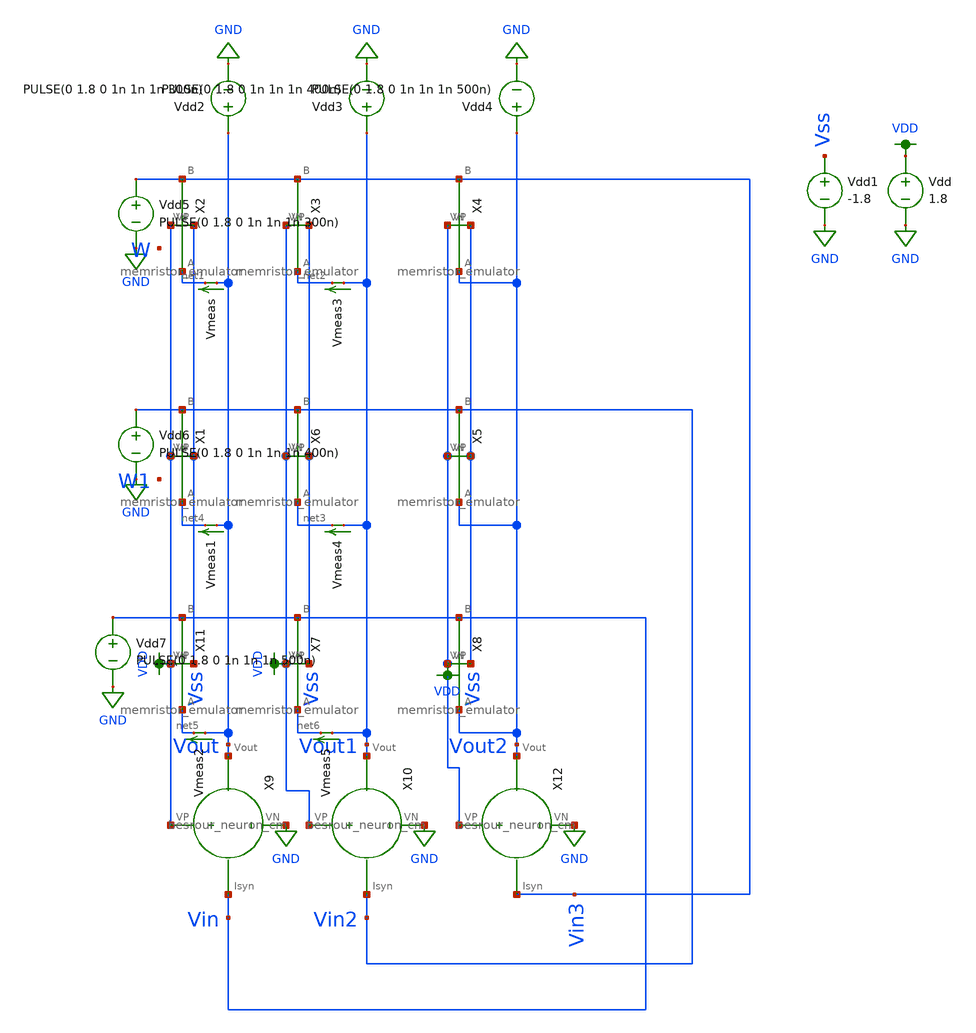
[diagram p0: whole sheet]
** sch_path: schematic/crossbar.sch
**.subckt crossbar
Vdd VDD GND 1.8
Vdd1 Vss GND -1.8
X11 VDD Vss Vin net5 memristor_emulator
X1 VDD Vss Vin2 net4 memristor_emulator
X2 VDD Vss Vin3 net1 memristor_emulator
X3 VDD Vss Vin3 net2 memristor_emulator
X4 VDD Vss Vin3 Vout2 memristor_emulator
X5 VDD Vss Vin2 Vout2 memristor_emulator
X6 VDD Vss Vin2 net3 memristor_emulator
X7 VDD Vss Vin net6 memristor_emulator
X8 VDD Vss Vin Vout2 memristor_emulator
X9 Vin Vout VDD GND besrour_neuron_cm
X10 Vin2 Vout1 VDD GND besrour_neuron_cm
X12 Vin3 Vout2 VDD GND besrour_neuron_cm
Vdd2 Vout GND PULSE(0 1.8 0 1n 1n 1n 300n)
Vdd3 Vout1 GND PULSE(0 1.8 0 1n 1n 1n 400n)
Vdd4 Vout2 GND PULSE(0 1.8 0 1n 1n 1n 500n)
Vdd5 Vin3 GND PULSE(0 1.8 0 1n 1n 1n 300n)
Vdd6 Vin2 GND PULSE(0 1.8 0 1n 1n 1n 400n)
Vdd7 Vin GND PULSE(0 1.8 0 1n 1n 1n 500n)
Vmeas Vout net1 0
.save i(vmeas)
Vmeas1 Vout net4 0
.save i(vmeas1)
Vmeas2 Vout net5 0
.save i(vmeas2)
Vmeas3 Vout1 net2 0
.save i(vmeas3)
Vmeas4 Vout1 net3 0
.save i(vmeas4)
Vmeas5 Vout1 net6 0
.save i(vmeas5)
**** begin user architecture code

.option wnflag=1
.param MC_SWITCH=0.0
.lib ~/skywater/skywater-pdk/libraries/sky130_fd_pr_ngspice/latest/models/sky130.lib.spice tt


.param W=12
.param L=0.5
.tran 1n 100u
.save all

**** end user architecture code
**.ends

* expanding   symbol:  /home/madvlsi/neuromorphic_computing_final/schematic/memristor_emulator.sym #
*+ of pins=4
** sym_path: schematic/memristor_emulator.sym
** sch_path: schematic/memristor_emulator.sch
.subckt memristor_emulator VP VN B A
*.ipin A
*.iopin VN
*.iopin VP
*.opin B
XM1 B in_cap A B sky130_fd_pr__pfet_01v8 L=0.3 W=12 nf=1 ad='int((nf+1)/2) * W/nf * 0.29' as='int((nf+2)/2) * W/nf * 0.29'
+ pd='2*int((nf+1)/2) * (W/nf + 0.29)' ps='2*int((nf+2)/2) * (W/nf + 0.29)' nrd='0.29 / W' nrs='0.29 / W'
+ sa=0 sb=0 sd=0 mult=1 m=1
XM2 VP A in_cap VP sky130_fd_pr__pfet_01v8 L=2 W=3 nf=1 ad='int((nf+1)/2) * W/nf * 0.29' as='int((nf+2)/2) * W/nf * 0.29'
+ pd='2*int((nf+1)/2) * (W/nf + 0.29)' ps='2*int((nf+2)/2) * (W/nf + 0.29)' nrd='0.29 / W' nrs='0.29 / W'
+ sa=0 sb=0 sd=0 mult=1 m=1
XM3 VN in_cap VN VN sky130_fd_pr__nfet_01v8 L=20 W=20 nf=1 ad='int((nf+1)/2) * W/nf * 0.29' as='int((nf+2)/2) * W/nf * 0.29'
+ pd='2*int((nf+1)/2) * (W/nf + 0.29)' ps='2*int((nf+2)/2) * (W/nf + 0.29)' nrd='0.29 / W' nrs='0.29 / W'
+ sa=0 sb=0 sd=0 mult=1 m=1
XM4 VN B in_cap VN sky130_fd_pr__nfet_01v8 L=3 W=2 nf=1 ad='int((nf+1)/2) * W/nf * 0.29' as='int((nf+2)/2) * W/nf * 0.29'
+ pd='2*int((nf+1)/2) * (W/nf + 0.29)' ps='2*int((nf+2)/2) * (W/nf + 0.29)' nrd='0.29 / W' nrs='0.29 / W'
+ sa=0 sb=0 sd=0 mult=1 m=1
.ends


* expanding   symbol:  /home/madvlsi/neuromorphic_computing_final/schematic/besrour_neuron_cm.sym #
*+ of pins=4
** sym_path: schematic/besrour_neuron_cm.sym
** sch_path: schematic/besrour_neuron_cm.sch
.subckt besrour_neuron_cm Isyn Vout VP VN
*.iopin VP
*.iopin VN
*.iopin Isyn
*.opin Vout
XM2 VMEMINT net1 VP VDD sky130_fd_pr__pfet_01v8 L={L} W={W} nf=1 ad='int((nf+1)/2) * W/nf * 0.29' as='int((nf+2)/2) * W/nf * 0.29'
+ pd='2*int((nf+1)/2) * (W/nf + 0.29)' ps='2*int((nf+2)/2) * (W/nf + 0.29)' nrd='0.29 / W' nrs='0.29 / W'
+ sa=0 sb=0 sd=0 mult=1 m=1
XM3 VP net3 VMEMINT VDD sky130_fd_pr__pfet_01v8 L={L} W={W} nf=1 ad='int((nf+1)/2) * W/nf * 0.29' as='int((nf+2)/2) * W/nf * 0.29'
+ pd='2*int((nf+1)/2) * (W/nf + 0.29)' ps='2*int((nf+2)/2) * (W/nf + 0.29)' nrd='0.29 / W' nrs='0.29 / W'
+ sa=0 sb=0 sd=0 mult=1 m=1
XM4 net3 VMEMINT VP VDD sky130_fd_pr__pfet_01v8 L={L} W={W} nf=1 ad='int((nf+1)/2) * W/nf * 0.29' as='int((nf+2)/2) * W/nf * 0.29'
+ pd='2*int((nf+1)/2) * (W/nf + 0.29)' ps='2*int((nf+2)/2) * (W/nf + 0.29)' nrd='0.29 / W' nrs='0.29 / W'
+ sa=0 sb=0 sd=0 mult=1 m=1
XM5 net2 net3 VP VDD sky130_fd_pr__pfet_01v8 L={L} W={W} nf=1 ad='int((nf+1)/2) * W/nf * 0.29' as='int((nf+2)/2) * W/nf * 0.29'
+ pd='2*int((nf+1)/2) * (W/nf + 0.29)' ps='2*int((nf+2)/2) * (W/nf + 0.29)' nrd='0.29 / W' nrs='0.29 / W'
+ sa=0 sb=0 sd=0 mult=1 m=1
XM6 net3 VMEMINT VN GND sky130_fd_pr__nfet_01v8 L={L} W={W} nf=1 ad='int((nf+1)/2) * W/nf * 0.29' as='int((nf+2)/2) * W/nf * 0.29'
+ pd='2*int((nf+1)/2) * (W/nf + 0.29)' ps='2*int((nf+2)/2) * (W/nf + 0.29)' nrd='0.29 / W' nrs='0.29 / W'
+ sa=0 sb=0 sd=0 mult=1 m=1
XM8 net2 net3 VN GND sky130_fd_pr__nfet_01v8 L={L} W={W} nf=1 ad='int((nf+1)/2) * W/nf * 0.29' as='int((nf+2)/2) * W/nf * 0.29'
+ pd='2*int((nf+1)/2) * (W/nf + 0.29)' ps='2*int((nf+2)/2) * (W/nf + 0.29)' nrd='0.29 / W' nrs='0.29 / W'
+ sa=0 sb=0 sd=0 mult=1 m=1
C1 VMEMINT VN 340f m=1
C2 net2 VN 340f m=1
XM9 net4 net2 VP VDD sky130_fd_pr__pfet_01v8 L={L} W={W} nf=1 ad='int((nf+1)/2) * W/nf * 0.29' as='int((nf+2)/2) * W/nf * 0.29'
+ pd='2*int((nf+1)/2) * (W/nf + 0.29)' ps='2*int((nf+2)/2) * (W/nf + 0.29)' nrd='0.29 / W' nrs='0.29 / W'
+ sa=0 sb=0 sd=0 mult=1 m=1
XM10 net4 net2 VN GND sky130_fd_pr__nfet_01v8 L={L} W={W} nf=1 ad='int((nf+1)/2) * W/nf * 0.29' as='int((nf+2)/2) * W/nf * 0.29'
+ pd='2*int((nf+1)/2) * (W/nf + 0.29)' ps='2*int((nf+2)/2) * (W/nf + 0.29)' nrd='0.29 / W' nrs='0.29 / W'
+ sa=0 sb=0 sd=0 mult=1 m=1
XM11 Vout net4 VP VDD sky130_fd_pr__pfet_01v8 L={L} W={W} nf=1 ad='int((nf+1)/2) * W/nf * 0.29' as='int((nf+2)/2) * W/nf * 0.29'
+ pd='2*int((nf+1)/2) * (W/nf + 0.29)' ps='2*int((nf+2)/2) * (W/nf + 0.29)' nrd='0.29 / W' nrs='0.29 / W'
+ sa=0 sb=0 sd=0 mult=1 m=1
XM12 Vout net4 VN GND sky130_fd_pr__nfet_01v8 L={L} W={W} nf=1 ad='int((nf+1)/2) * W/nf * 0.29' as='int((nf+2)/2) * W/nf * 0.29'
+ pd='2*int((nf+1)/2) * (W/nf + 0.29)' ps='2*int((nf+2)/2) * (W/nf + 0.29)' nrd='0.29 / W' nrs='0.29 / W'
+ sa=0 sb=0 sd=0 mult=1 m=1
XM13 net1 Isyn VN GND sky130_fd_pr__nfet_01v8 L={L} W={W} nf=1 ad='int((nf+1)/2) * W/nf * 0.29' as='int((nf+2)/2) * W/nf * 0.29'
+ pd='2*int((nf+1)/2) * (W/nf + 0.29)' ps='2*int((nf+2)/2) * (W/nf + 0.29)' nrd='0.29 / W' nrs='0.29 / W'
+ sa=0 sb=0 sd=0 mult=1 m=1
XM14 VN Isyn Isyn GND sky130_fd_pr__nfet_01v8 L={L} W={W} nf=1 ad='int((nf+1)/2) * W/nf * 0.29' as='int((nf+2)/2) * W/nf * 0.29'
+ pd='2*int((nf+1)/2) * (W/nf + 0.29)' ps='2*int((nf+2)/2) * (W/nf + 0.29)' nrd='0.29 / W' nrs='0.29 / W'
+ sa=0 sb=0 sd=0 mult=1 m=1
XM1 VP net1 net1 VDD sky130_fd_pr__pfet_01v8 L={L} W={W} nf=1 ad='int((nf+1)/2) * W/nf * 0.29' as='int((nf+2)/2) * W/nf * 0.29'
+ pd='2*int((nf+1)/2) * (W/nf + 0.29)' ps='2*int((nf+2)/2) * (W/nf + 0.29)' nrd='0.29 / W' nrs='0.29 / W'
+ sa=0 sb=0 sd=0 mult=1 m=1
XM7 VN net2 VMEMINT GND sky130_fd_pr__nfet_01v8 L={L} W={W} nf=1 ad='int((nf+1)/2) * W/nf * 0.29' as='int((nf+2)/2) * W/nf * 0.29'
+ pd='2*int((nf+1)/2) * (W/nf + 0.29)' ps='2*int((nf+2)/2) * (W/nf + 0.29)' nrd='0.29 / W' nrs='0.29 / W'
+ sa=0 sb=0 sd=0 mult=1 m=1
.ends

.GLOBAL VDD
.GLOBAL GND
.end
